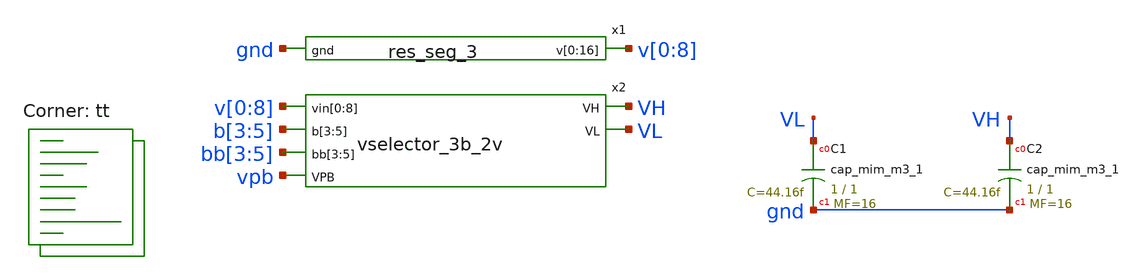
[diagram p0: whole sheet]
** sch_path: xschem/res_seg_3-tb.sch
**.subckt res_seg_3-tb
x1 v[0] v[1] v[2] v[3] v[4] v[5] v[6] v[7] v[8] v[0] v[1] v[2] v[3] v[4] v[5] v[6] v[7] gnd
+ res_seg_3
x2 v[0] v[1] v[2] v[3] v[4] v[5] v[6] v[7] v[8] b[3] b[4] b[5] bb[3] bb[4] bb[5] VH VL vpb
+ vselector_3b_2v
XC1 VL gnd sky130_fd_pr__cap_mim_m3_1 W=1 L=1 MF=16 m=16
XC2 VH gnd sky130_fd_pr__cap_mim_m3_1 W=1 L=1 MF=16 m=16
**** begin user architecture code



  .option wnflag=1
  .option safecurrents
  ********************Static Voltage Sources***************************
  Vddh vddh gnd dc 5.5
  Vpb  vpb  gnd dc 5.5

  V8 v[8] gnd dc 4.719
  v0 v[0] gnd dc 4.3209
  ********************Dynamic Voltage Sources***************************
  *******Calculation**********
  .param base_f=100e3 base_t={1/base_f} base_th={base_t/2} base_d={base_th}
  .param b3_th={base_th} b3_t={b3_th*2}
  .param b4_th={b3_th*2} b4_t={b4_th*2}
  .param b5_th={b4_th*2} b5_t={b5_th*2}
  *******Signals**********
  .param vhi=5.5
  Vb3  b[3]  gnd pulse({vhi} 0 {base_d} 1n 1n {b3_th} {b3_t})
  Vb4  b[4]  gnd pulse({vhi} 0 {base_d} 1n 1n {b4_th} {b4_t})
  Vb5  b[5]  gnd pulse({vhi} 0 {base_d} 1n 1n {b5_th} {b5_t})

  Vbb3  bb[3]  gnd pulse(0 {vhi} {base_d} 1n 1n {b3_th} {b3_t})
  Vbb4  bb[4]  gnd pulse(0 {vhi} {base_d} 1n 1n {b4_th} {b4_t})
  Vbb5  bb[5]  gnd pulse(0 {vhi} {base_d} 1n 1n {b5_th} {b5_t})
  ********************Simulation Commands*****************************
  .control
     reset
     save all
     tran 1n 100u
     write res_seg_3-tb.raw
     set appendwrite
*    quit 0
  .endc



.lib $::SKYWATER_MODELS/sky130.lib.spice tt
**** end user architecture code
**.ends

* expanding   symbol:  res_seg_3.sym # of pins=2
** sym_path: xschem/res_seg_3.sym
** sch_path: xschem/res_seg_3.sch
.subckt res_seg_3 v[0] v[1] v[2] v[3] v[4] v[5] v[6] v[7] v[8] v[9] v[10] v[11] v[12] v[13] v[14]
+ v[15] v[16] gnd
*.opin v[0],v[1],v[2],v[3],v[4],v[5],v[6],v[7],v[8],v[9],v[10],v[11],v[12],v[13],v[14],v[15],v[16]
*.ipin gnd
XR1 v[0] v[1] gnd sky130_fd_pr__res_xhigh_po_0p35 L=0.5555 mult=1 m=1
XR2 v[1] v[2] gnd sky130_fd_pr__res_xhigh_po_0p35 L=0.5726 mult=1 m=1
XR3 v[2] v[3] gnd sky130_fd_pr__res_xhigh_po_0p35 L=0.5811 mult=1 m=1
XR4 v[3] v[4] gnd sky130_fd_pr__res_xhigh_po_0p35 L=0.5897 mult=1 m=1
XR5 v[4] v[5] gnd sky130_fd_pr__res_xhigh_po_0p35 L=0.6153 mult=1 m=1
XR6 v[5] v[6] gnd sky130_fd_pr__res_xhigh_po_0p35 L=0.6238 mult=1 m=1
XR7 v[6] v[7] gnd sky130_fd_pr__res_xhigh_po_0p35 L=0.6409 mult=1 m=1
XR8 v[7] v[8] gnd sky130_fd_pr__res_xhigh_po_0p35 L=0.6666 mult=1 m=1
XR9 v[8] v[9] gnd sky130_fd_pr__res_xhigh_po_0p35 L=0.6837 mult=1 m=1
XR10 v[9] v[10] gnd sky130_fd_pr__res_xhigh_po_0p35 L=0.7093 mult=1 m=1
XR11 v[10] v[11] gnd sky130_fd_pr__res_xhigh_po_0p35 L=0.7264 mult=1 m=1
XR12 v[11] v[12] gnd sky130_fd_pr__res_xhigh_po_0p35 L=0.7691 mult=1 m=1
XR13 v[12] v[13] gnd sky130_fd_pr__res_xhigh_po_0p35 L=0.7948 mult=1 m=1
XR14 v[13] v[14] gnd sky130_fd_pr__res_xhigh_po_0p35 L=0.8375 mult=1 m=1
XR15 v[14] v[15] gnd sky130_fd_pr__res_xhigh_po_0p35 L=0.8802 mult=1 m=1
XR16 v[15] v[16] gnd sky130_fd_pr__res_xhigh_po_0p35 L=0.9315 mult=1 m=1
.ends


* expanding   symbol:  vselector_3b_2v.sym # of pins=6
** sym_path: xschem/vselector_3b_2v.sym
** sch_path: xschem/vselector_3b_2v.sch
.subckt vselector_3b_2v vin[0] vin[1] vin[2] vin[3] vin[4] vin[5] vin[6] vin[7] vin[8] b[3] b[4]
+ b[5] bb[3] bb[4] bb[5] VH VL VPB
*.ipin vin[0],vin[1],vin[2],vin[3],vin[4],vin[5],vin[6],vin[7],vin[8]
*.opin VH
*.ipin VPB
*.ipin b[3],b[4],b[5]
*.opin VL
*.ipin bb[3],bb[4],bb[5]
XM1 v5[0] b[5] vin[0] VPB sky130_fd_pr__pfet_g5v0d10v5 L=l W=wp nf=1 ad='int((nf+1)/2) * W/nf * 0.29'
+ as='int((nf+2)/2) * W/nf * 0.29' pd='2*int((nf+1)/2) * (W/nf + 0.29)' ps='2*int((nf+2)/2) * (W/nf + 0.29)'
+ nrd='0.29 / W' nrs='0.29 / W' sa=0 sb=0 sd=0 mult=1 m=1
.param wp=0.42 wn=0.42 l=0.5

XM2 v5[1] b[5] vin[1] VPB sky130_fd_pr__pfet_g5v0d10v5 L=l W=wp nf=1 ad='int((nf+1)/2) * W/nf * 0.29'
+ as='int((nf+2)/2) * W/nf * 0.29' pd='2*int((nf+1)/2) * (W/nf + 0.29)' ps='2*int((nf+2)/2) * (W/nf + 0.29)'
+ nrd='0.29 / W' nrs='0.29 / W' sa=0 sb=0 sd=0 mult=1 m=1
XM3 v5[2] b[5] vin[2] VPB sky130_fd_pr__pfet_g5v0d10v5 L=l W=wp nf=1 ad='int((nf+1)/2) * W/nf * 0.29'
+ as='int((nf+2)/2) * W/nf * 0.29' pd='2*int((nf+1)/2) * (W/nf + 0.29)' ps='2*int((nf+2)/2) * (W/nf + 0.29)'
+ nrd='0.29 / W' nrs='0.29 / W' sa=0 sb=0 sd=0 mult=1 m=1
XM4 v5[3] b[5] vin[3] VPB sky130_fd_pr__pfet_g5v0d10v5 L=l W=wp nf=1 ad='int((nf+1)/2) * W/nf * 0.29'
+ as='int((nf+2)/2) * W/nf * 0.29' pd='2*int((nf+1)/2) * (W/nf + 0.29)' ps='2*int((nf+2)/2) * (W/nf + 0.29)'
+ nrd='0.29 / W' nrs='0.29 / W' sa=0 sb=0 sd=0 mult=1 m=1
XM5 v5[4] b[5] vin[4] VPB sky130_fd_pr__pfet_g5v0d10v5 L=l W=wp nf=1 ad='int((nf+1)/2) * W/nf * 0.29'
+ as='int((nf+2)/2) * W/nf * 0.29' pd='2*int((nf+1)/2) * (W/nf + 0.29)' ps='2*int((nf+2)/2) * (W/nf + 0.29)'
+ nrd='0.29 / W' nrs='0.29 / W' sa=0 sb=0 sd=0 mult=1 m=1
XM11 v4[0] b[4] v5[0] VPB sky130_fd_pr__pfet_g5v0d10v5 L=l W=wp nf=1 ad='int((nf+1)/2) * W/nf * 0.29'
+ as='int((nf+2)/2) * W/nf * 0.29' pd='2*int((nf+1)/2) * (W/nf + 0.29)' ps='2*int((nf+2)/2) * (W/nf + 0.29)'
+ nrd='0.29 / W' nrs='0.29 / W' sa=0 sb=0 sd=0 mult=1 m=1
XM12 v4[1] b[4] v5[1] VPB sky130_fd_pr__pfet_g5v0d10v5 L=l W=wp nf=1 ad='int((nf+1)/2) * W/nf * 0.29'
+ as='int((nf+2)/2) * W/nf * 0.29' pd='2*int((nf+1)/2) * (W/nf + 0.29)' ps='2*int((nf+2)/2) * (W/nf + 0.29)'
+ nrd='0.29 / W' nrs='0.29 / W' sa=0 sb=0 sd=0 mult=1 m=1
XM13 v4[2] b[4] v5[2] VPB sky130_fd_pr__pfet_g5v0d10v5 L=l W=wp nf=1 ad='int((nf+1)/2) * W/nf * 0.29'
+ as='int((nf+2)/2) * W/nf * 0.29' pd='2*int((nf+1)/2) * (W/nf + 0.29)' ps='2*int((nf+2)/2) * (W/nf + 0.29)'
+ nrd='0.29 / W' nrs='0.29 / W' sa=0 sb=0 sd=0 mult=1 m=1
XM17 VL b[3] v4[0] VPB sky130_fd_pr__pfet_g5v0d10v5 L=l W=wp nf=1 ad='int((nf+1)/2) * W/nf * 0.29' as='int((nf+2)/2) * W/nf * 0.29'
+ pd='2*int((nf+1)/2) * (W/nf + 0.29)' ps='2*int((nf+2)/2) * (W/nf + 0.29)' nrd='0.29 / W' nrs='0.29 / W'
+ sa=0 sb=0 sd=0 mult=1 m=1
XM19 VH b[3] v4[1] VPB sky130_fd_pr__pfet_g5v0d10v5 L=l W=wp nf=1 ad='int((nf+1)/2) * W/nf * 0.29' as='int((nf+2)/2) * W/nf * 0.29'
+ pd='2*int((nf+1)/2) * (W/nf + 0.29)' ps='2*int((nf+2)/2) * (W/nf + 0.29)' nrd='0.29 / W' nrs='0.29 / W'
+ sa=0 sb=0 sd=0 mult=1 m=1
XM6 v5[0] bb[5] vin[4] VPB sky130_fd_pr__pfet_g5v0d10v5 L=l W=wp nf=1 ad='int((nf+1)/2) * W/nf * 0.29'
+ as='int((nf+2)/2) * W/nf * 0.29' pd='2*int((nf+1)/2) * (W/nf + 0.29)' ps='2*int((nf+2)/2) * (W/nf + 0.29)'
+ nrd='0.29 / W' nrs='0.29 / W' sa=0 sb=0 sd=0 mult=1 m=1
XM7 v5[1] bb[5] vin[5] VPB sky130_fd_pr__pfet_g5v0d10v5 L=l W=wp nf=1 ad='int((nf+1)/2) * W/nf * 0.29'
+ as='int((nf+2)/2) * W/nf * 0.29' pd='2*int((nf+1)/2) * (W/nf + 0.29)' ps='2*int((nf+2)/2) * (W/nf + 0.29)'
+ nrd='0.29 / W' nrs='0.29 / W' sa=0 sb=0 sd=0 mult=1 m=1
XM8 v5[2] bb[5] vin[6] VPB sky130_fd_pr__pfet_g5v0d10v5 L=l W=wp nf=1 ad='int((nf+1)/2) * W/nf * 0.29'
+ as='int((nf+2)/2) * W/nf * 0.29' pd='2*int((nf+1)/2) * (W/nf + 0.29)' ps='2*int((nf+2)/2) * (W/nf + 0.29)'
+ nrd='0.29 / W' nrs='0.29 / W' sa=0 sb=0 sd=0 mult=1 m=1
XM9 v5[3] bb[5] vin[7] VPB sky130_fd_pr__pfet_g5v0d10v5 L=l W=wp nf=1 ad='int((nf+1)/2) * W/nf * 0.29'
+ as='int((nf+2)/2) * W/nf * 0.29' pd='2*int((nf+1)/2) * (W/nf + 0.29)' ps='2*int((nf+2)/2) * (W/nf + 0.29)'
+ nrd='0.29 / W' nrs='0.29 / W' sa=0 sb=0 sd=0 mult=1 m=1
XM10 v5[4] bb[5] vin[8] VPB sky130_fd_pr__pfet_g5v0d10v5 L=l W=wp nf=1 ad='int((nf+1)/2) * W/nf * 0.29'
+ as='int((nf+2)/2) * W/nf * 0.29' pd='2*int((nf+1)/2) * (W/nf + 0.29)' ps='2*int((nf+2)/2) * (W/nf + 0.29)'
+ nrd='0.29 / W' nrs='0.29 / W' sa=0 sb=0 sd=0 mult=1 m=1
XM14 v4[0] bb[4] v5[2] VPB sky130_fd_pr__pfet_g5v0d10v5 L=l W=wp nf=1 ad='int((nf+1)/2) * W/nf * 0.29'
+ as='int((nf+2)/2) * W/nf * 0.29' pd='2*int((nf+1)/2) * (W/nf + 0.29)' ps='2*int((nf+2)/2) * (W/nf + 0.29)'
+ nrd='0.29 / W' nrs='0.29 / W' sa=0 sb=0 sd=0 mult=1 m=1
XM15 v4[1] bb[4] v5[3] VPB sky130_fd_pr__pfet_g5v0d10v5 L=l W=wp nf=1 ad='int((nf+1)/2) * W/nf * 0.29'
+ as='int((nf+2)/2) * W/nf * 0.29' pd='2*int((nf+1)/2) * (W/nf + 0.29)' ps='2*int((nf+2)/2) * (W/nf + 0.29)'
+ nrd='0.29 / W' nrs='0.29 / W' sa=0 sb=0 sd=0 mult=1 m=1
XM16 v4[2] bb[4] v5[4] VPB sky130_fd_pr__pfet_g5v0d10v5 L=l W=wp nf=1 ad='int((nf+1)/2) * W/nf * 0.29'
+ as='int((nf+2)/2) * W/nf * 0.29' pd='2*int((nf+1)/2) * (W/nf + 0.29)' ps='2*int((nf+2)/2) * (W/nf + 0.29)'
+ nrd='0.29 / W' nrs='0.29 / W' sa=0 sb=0 sd=0 mult=1 m=1
XM18 VL bb[3] v4[1] VPB sky130_fd_pr__pfet_g5v0d10v5 L=l W=wp nf=1 ad='int((nf+1)/2) * W/nf * 0.29' as='int((nf+2)/2) * W/nf * 0.29'
+ pd='2*int((nf+1)/2) * (W/nf + 0.29)' ps='2*int((nf+2)/2) * (W/nf + 0.29)' nrd='0.29 / W' nrs='0.29 / W'
+ sa=0 sb=0 sd=0 mult=1 m=1
XM20 VH bb[3] v4[2] VPB sky130_fd_pr__pfet_g5v0d10v5 L=l W=wp nf=1 ad='int((nf+1)/2) * W/nf * 0.29' as='int((nf+2)/2) * W/nf * 0.29'
+ pd='2*int((nf+1)/2) * (W/nf + 0.29)' ps='2*int((nf+2)/2) * (W/nf + 0.29)' nrd='0.29 / W' nrs='0.29 / W'
+ sa=0 sb=0 sd=0 mult=1 m=1
.ends

.end
